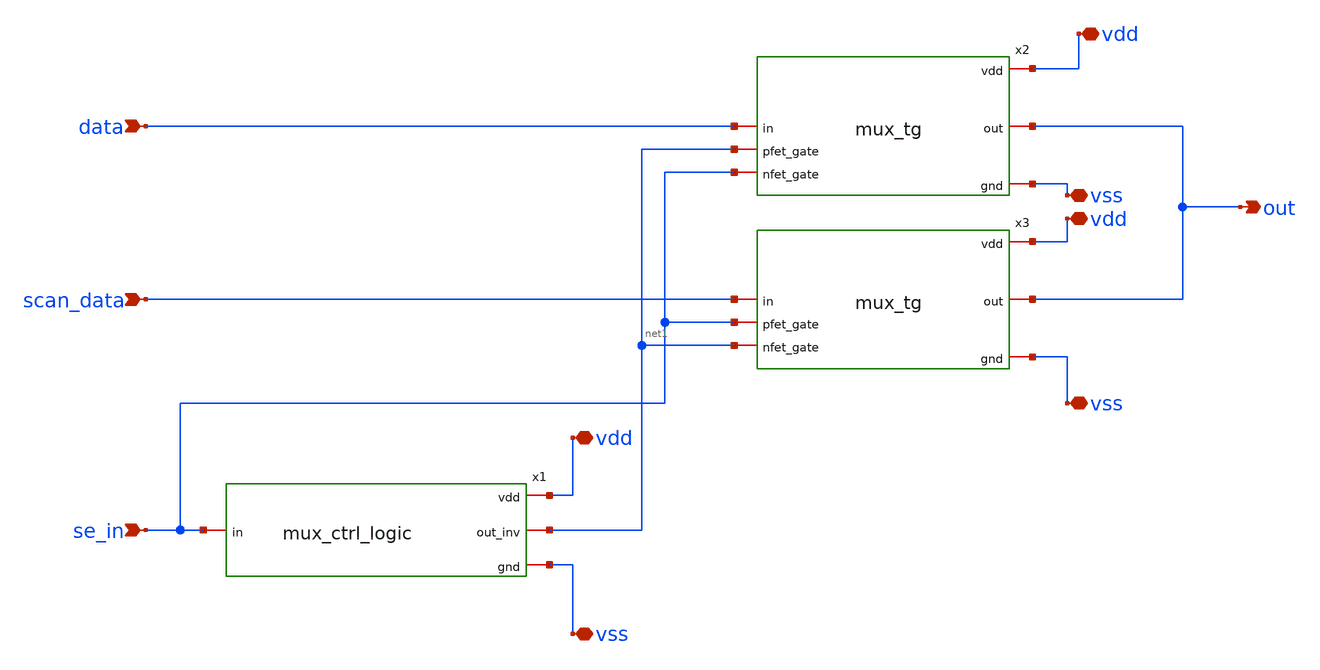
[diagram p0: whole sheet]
** sch_path: designs/schematics/mux2x1_transmission_gate/mux_toplevel.sch
**.subckt mux_toplevel vdd out data scan_data se_in vdd vss vss vdd vss
*.iopin vdd
*.opin out
*.ipin data
*.ipin scan_data
*.ipin se_in
*.iopin vdd
*.iopin vss
*.iopin vss
*.iopin vdd
*.iopin vss
x2 vdd net1 data out se_in vss mux_tg
x3 vdd se_in scan_data out net1 vss mux_tg
x1 vdd se_in net1 vss mux_ctrl_logic
**.ends

* expanding   symbol:  schematics/mux2x1_transmission_gate/mux_tg.sym # of pins=6
** sym_path: designs/schematics/mux2x1_transmission_gate/mux_tg.sym
** sch_path: designs/schematics/mux2x1_transmission_gate/mux_tg.sch
.subckt mux_tg vdd pfet_gate in out nfet_gate gnd
*.iopin vdd
*.iopin gnd
*.iopin out
*.iopin in
*.iopin pfet_gate
*.iopin nfet_gate
XM1 in nfet_gate out gnd nfet_03v3 L=0.28u W=0.22u nf=1 ad='int((nf+1)/2) * W/nf * 0.18u' as='int((nf+2)/2) * W/nf * 0.18u'
+ pd='2*int((nf+1)/2) * (W/nf + 0.18u)' ps='2*int((nf+2)/2) * (W/nf + 0.18u)' nrd='0.18u / W' nrs='0.18u / W'
+ sa=0 sb=0 sd=0 m=1
XM2 in pfet_gate out vdd pfet_03v3 L=0.28u W=0.22u nf=1 ad='int((nf+1)/2) * W/nf * 0.18u' as='int((nf+2)/2) * W/nf * 0.18u'
+ pd='2*int((nf+1)/2) * (W/nf + 0.18u)' ps='2*int((nf+2)/2) * (W/nf + 0.18u)' nrd='0.18u / W' nrs='0.18u / W'
+ sa=0 sb=0 sd=0 m=1
.ends


* expanding   symbol:  schematics/mux2x1_transmission_gate/mux_ctrl_logic.sym # of pins=4
** sym_path: designs/schematics/mux2x1_transmission_gate/mux_ctrl_logic.sym
** sch_path: designs/schematics/mux2x1_transmission_gate/mux_ctrl_logic.sch
.subckt mux_ctrl_logic vdd in out_inv gnd
*.iopin vdd
*.iopin gnd
*.iopin out_inv
*.iopin in
XM1 out_inv in gnd gnd nfet_03v3 L=0.28u W=0.22u nf=1 ad='int((nf+1)/2) * W/nf * 0.18u' as='int((nf+2)/2) * W/nf * 0.18u'
+ pd='2*int((nf+1)/2) * (W/nf + 0.18u)' ps='2*int((nf+2)/2) * (W/nf + 0.18u)' nrd='0.18u / W' nrs='0.18u / W'
+ sa=0 sb=0 sd=0 m=1
XM2 out_inv in vdd vdd pfet_03v3 L=0.28u W=0.22u nf=1 ad='int((nf+1)/2) * W/nf * 0.18u' as='int((nf+2)/2) * W/nf * 0.18u'
+ pd='2*int((nf+1)/2) * (W/nf + 0.18u)' ps='2*int((nf+2)/2) * (W/nf + 0.18u)' nrd='0.18u / W' nrs='0.18u / W'
+ sa=0 sb=0 sd=0 m=1
.ends

.end
